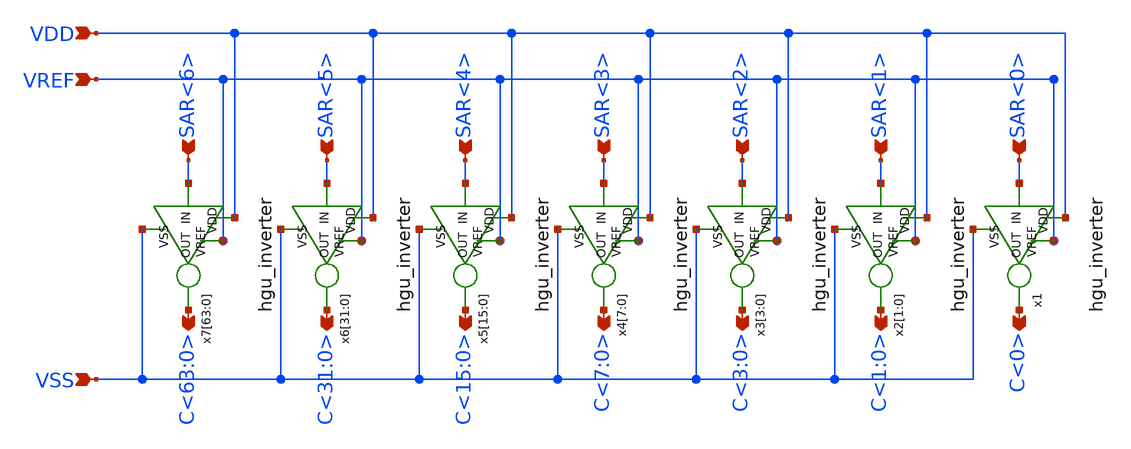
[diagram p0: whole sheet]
** sch_path: hgu/xschem/hgu_cdac_drv.sch
**.subckt hgu_cdac_drv VREF VSS SAR<6> SAR<5> SAR<4> SAR<3> SAR<2> SAR<1> SAR<0> C<63:0> C<31:0>
*+ C<15:0> C<7:0> C<3:0> C<1:0> C<0> VDD
*.ipin VREF
*.ipin VSS
*.ipin SAR<6>
*.ipin SAR<5>
*.ipin SAR<4>
*.ipin SAR<3>
*.ipin SAR<2>
*.ipin SAR<1>
*.ipin SAR<0>
*.opin C<63:0>
*.opin C<31:0>
*.opin C<15:0>
*.opin C<7:0>
*.opin C<3:0>
*.opin C<1:0>
*.opin C<0>
*.ipin VDD
x7[63] VDD SAR<6> C<63:0> VSS VREF hgu_inverter
x7[62] VDD SAR<6> C<63:0> VSS VREF hgu_inverter
x7[61] VDD SAR<6> C<63:0> VSS VREF hgu_inverter
x7[60] VDD SAR<6> C<63:0> VSS VREF hgu_inverter
x7[59] VDD SAR<6> C<63:0> VSS VREF hgu_inverter
x7[58] VDD SAR<6> C<63:0> VSS VREF hgu_inverter
x7[57] VDD SAR<6> C<63:0> VSS VREF hgu_inverter
x7[56] VDD SAR<6> C<63:0> VSS VREF hgu_inverter
x7[55] VDD SAR<6> C<63:0> VSS VREF hgu_inverter
x7[54] VDD SAR<6> C<63:0> VSS VREF hgu_inverter
x7[53] VDD SAR<6> C<63:0> VSS VREF hgu_inverter
x7[52] VDD SAR<6> C<63:0> VSS VREF hgu_inverter
x7[51] VDD SAR<6> C<63:0> VSS VREF hgu_inverter
x7[50] VDD SAR<6> C<63:0> VSS VREF hgu_inverter
x7[49] VDD SAR<6> C<63:0> VSS VREF hgu_inverter
x7[48] VDD SAR<6> C<63:0> VSS VREF hgu_inverter
x7[47] VDD SAR<6> C<63:0> VSS VREF hgu_inverter
x7[46] VDD SAR<6> C<63:0> VSS VREF hgu_inverter
x7[45] VDD SAR<6> C<63:0> VSS VREF hgu_inverter
x7[44] VDD SAR<6> C<63:0> VSS VREF hgu_inverter
x7[43] VDD SAR<6> C<63:0> VSS VREF hgu_inverter
x7[42] VDD SAR<6> C<63:0> VSS VREF hgu_inverter
x7[41] VDD SAR<6> C<63:0> VSS VREF hgu_inverter
x7[40] VDD SAR<6> C<63:0> VSS VREF hgu_inverter
x7[39] VDD SAR<6> C<63:0> VSS VREF hgu_inverter
x7[38] VDD SAR<6> C<63:0> VSS VREF hgu_inverter
x7[37] VDD SAR<6> C<63:0> VSS VREF hgu_inverter
x7[36] VDD SAR<6> C<63:0> VSS VREF hgu_inverter
x7[35] VDD SAR<6> C<63:0> VSS VREF hgu_inverter
x7[34] VDD SAR<6> C<63:0> VSS VREF hgu_inverter
x7[33] VDD SAR<6> C<63:0> VSS VREF hgu_inverter
x7[32] VDD SAR<6> C<63:0> VSS VREF hgu_inverter
x7[31] VDD SAR<6> C<63:0> VSS VREF hgu_inverter
x7[30] VDD SAR<6> C<63:0> VSS VREF hgu_inverter
x7[29] VDD SAR<6> C<63:0> VSS VREF hgu_inverter
x7[28] VDD SAR<6> C<63:0> VSS VREF hgu_inverter
x7[27] VDD SAR<6> C<63:0> VSS VREF hgu_inverter
x7[26] VDD SAR<6> C<63:0> VSS VREF hgu_inverter
x7[25] VDD SAR<6> C<63:0> VSS VREF hgu_inverter
x7[24] VDD SAR<6> C<63:0> VSS VREF hgu_inverter
x7[23] VDD SAR<6> C<63:0> VSS VREF hgu_inverter
x7[22] VDD SAR<6> C<63:0> VSS VREF hgu_inverter
x7[21] VDD SAR<6> C<63:0> VSS VREF hgu_inverter
x7[20] VDD SAR<6> C<63:0> VSS VREF hgu_inverter
x7[19] VDD SAR<6> C<63:0> VSS VREF hgu_inverter
x7[18] VDD SAR<6> C<63:0> VSS VREF hgu_inverter
x7[17] VDD SAR<6> C<63:0> VSS VREF hgu_inverter
x7[16] VDD SAR<6> C<63:0> VSS VREF hgu_inverter
x7[15] VDD SAR<6> C<63:0> VSS VREF hgu_inverter
x7[14] VDD SAR<6> C<63:0> VSS VREF hgu_inverter
x7[13] VDD SAR<6> C<63:0> VSS VREF hgu_inverter
x7[12] VDD SAR<6> C<63:0> VSS VREF hgu_inverter
x7[11] VDD SAR<6> C<63:0> VSS VREF hgu_inverter
x7[10] VDD SAR<6> C<63:0> VSS VREF hgu_inverter
x7[9] VDD SAR<6> C<63:0> VSS VREF hgu_inverter
x7[8] VDD SAR<6> C<63:0> VSS VREF hgu_inverter
x7[7] VDD SAR<6> C<63:0> VSS VREF hgu_inverter
x7[6] VDD SAR<6> C<63:0> VSS VREF hgu_inverter
x7[5] VDD SAR<6> C<63:0> VSS VREF hgu_inverter
x7[4] VDD SAR<6> C<63:0> VSS VREF hgu_inverter
x7[3] VDD SAR<6> C<63:0> VSS VREF hgu_inverter
x7[2] VDD SAR<6> C<63:0> VSS VREF hgu_inverter
x7[1] VDD SAR<6> C<63:0> VSS VREF hgu_inverter
x7[0] VDD SAR<6> C<63:0> VSS VREF hgu_inverter
x1 VDD SAR<0> C<0> VSS VREF hgu_inverter
x2[1] VDD SAR<1> C<1:0> VSS VREF hgu_inverter
x2[0] VDD SAR<1> C<1:0> VSS VREF hgu_inverter
x3[3] VDD SAR<2> C<3:0> VSS VREF hgu_inverter
x3[2] VDD SAR<2> C<3:0> VSS VREF hgu_inverter
x3[1] VDD SAR<2> C<3:0> VSS VREF hgu_inverter
x3[0] VDD SAR<2> C<3:0> VSS VREF hgu_inverter
x4[7] VDD SAR<3> C<7:0> VSS VREF hgu_inverter
x4[6] VDD SAR<3> C<7:0> VSS VREF hgu_inverter
x4[5] VDD SAR<3> C<7:0> VSS VREF hgu_inverter
x4[4] VDD SAR<3> C<7:0> VSS VREF hgu_inverter
x4[3] VDD SAR<3> C<7:0> VSS VREF hgu_inverter
x4[2] VDD SAR<3> C<7:0> VSS VREF hgu_inverter
x4[1] VDD SAR<3> C<7:0> VSS VREF hgu_inverter
x4[0] VDD SAR<3> C<7:0> VSS VREF hgu_inverter
x5[15] VDD SAR<4> C<15:0> VSS VREF hgu_inverter
x5[14] VDD SAR<4> C<15:0> VSS VREF hgu_inverter
x5[13] VDD SAR<4> C<15:0> VSS VREF hgu_inverter
x5[12] VDD SAR<4> C<15:0> VSS VREF hgu_inverter
x5[11] VDD SAR<4> C<15:0> VSS VREF hgu_inverter
x5[10] VDD SAR<4> C<15:0> VSS VREF hgu_inverter
x5[9] VDD SAR<4> C<15:0> VSS VREF hgu_inverter
x5[8] VDD SAR<4> C<15:0> VSS VREF hgu_inverter
x5[7] VDD SAR<4> C<15:0> VSS VREF hgu_inverter
x5[6] VDD SAR<4> C<15:0> VSS VREF hgu_inverter
x5[5] VDD SAR<4> C<15:0> VSS VREF hgu_inverter
x5[4] VDD SAR<4> C<15:0> VSS VREF hgu_inverter
x5[3] VDD SAR<4> C<15:0> VSS VREF hgu_inverter
x5[2] VDD SAR<4> C<15:0> VSS VREF hgu_inverter
x5[1] VDD SAR<4> C<15:0> VSS VREF hgu_inverter
x5[0] VDD SAR<4> C<15:0> VSS VREF hgu_inverter
x6[31] VDD SAR<5> C<31:0> VSS VREF hgu_inverter
x6[30] VDD SAR<5> C<31:0> VSS VREF hgu_inverter
x6[29] VDD SAR<5> C<31:0> VSS VREF hgu_inverter
x6[28] VDD SAR<5> C<31:0> VSS VREF hgu_inverter
x6[27] VDD SAR<5> C<31:0> VSS VREF hgu_inverter
x6[26] VDD SAR<5> C<31:0> VSS VREF hgu_inverter
x6[25] VDD SAR<5> C<31:0> VSS VREF hgu_inverter
x6[24] VDD SAR<5> C<31:0> VSS VREF hgu_inverter
x6[23] VDD SAR<5> C<31:0> VSS VREF hgu_inverter
x6[22] VDD SAR<5> C<31:0> VSS VREF hgu_inverter
x6[21] VDD SAR<5> C<31:0> VSS VREF hgu_inverter
x6[20] VDD SAR<5> C<31:0> VSS VREF hgu_inverter
x6[19] VDD SAR<5> C<31:0> VSS VREF hgu_inverter
x6[18] VDD SAR<5> C<31:0> VSS VREF hgu_inverter
x6[17] VDD SAR<5> C<31:0> VSS VREF hgu_inverter
x6[16] VDD SAR<5> C<31:0> VSS VREF hgu_inverter
x6[15] VDD SAR<5> C<31:0> VSS VREF hgu_inverter
x6[14] VDD SAR<5> C<31:0> VSS VREF hgu_inverter
x6[13] VDD SAR<5> C<31:0> VSS VREF hgu_inverter
x6[12] VDD SAR<5> C<31:0> VSS VREF hgu_inverter
x6[11] VDD SAR<5> C<31:0> VSS VREF hgu_inverter
x6[10] VDD SAR<5> C<31:0> VSS VREF hgu_inverter
x6[9] VDD SAR<5> C<31:0> VSS VREF hgu_inverter
x6[8] VDD SAR<5> C<31:0> VSS VREF hgu_inverter
x6[7] VDD SAR<5> C<31:0> VSS VREF hgu_inverter
x6[6] VDD SAR<5> C<31:0> VSS VREF hgu_inverter
x6[5] VDD SAR<5> C<31:0> VSS VREF hgu_inverter
x6[4] VDD SAR<5> C<31:0> VSS VREF hgu_inverter
x6[3] VDD SAR<5> C<31:0> VSS VREF hgu_inverter
x6[2] VDD SAR<5> C<31:0> VSS VREF hgu_inverter
x6[1] VDD SAR<5> C<31:0> VSS VREF hgu_inverter
x6[0] VDD SAR<5> C<31:0> VSS VREF hgu_inverter
**.ends
.end
